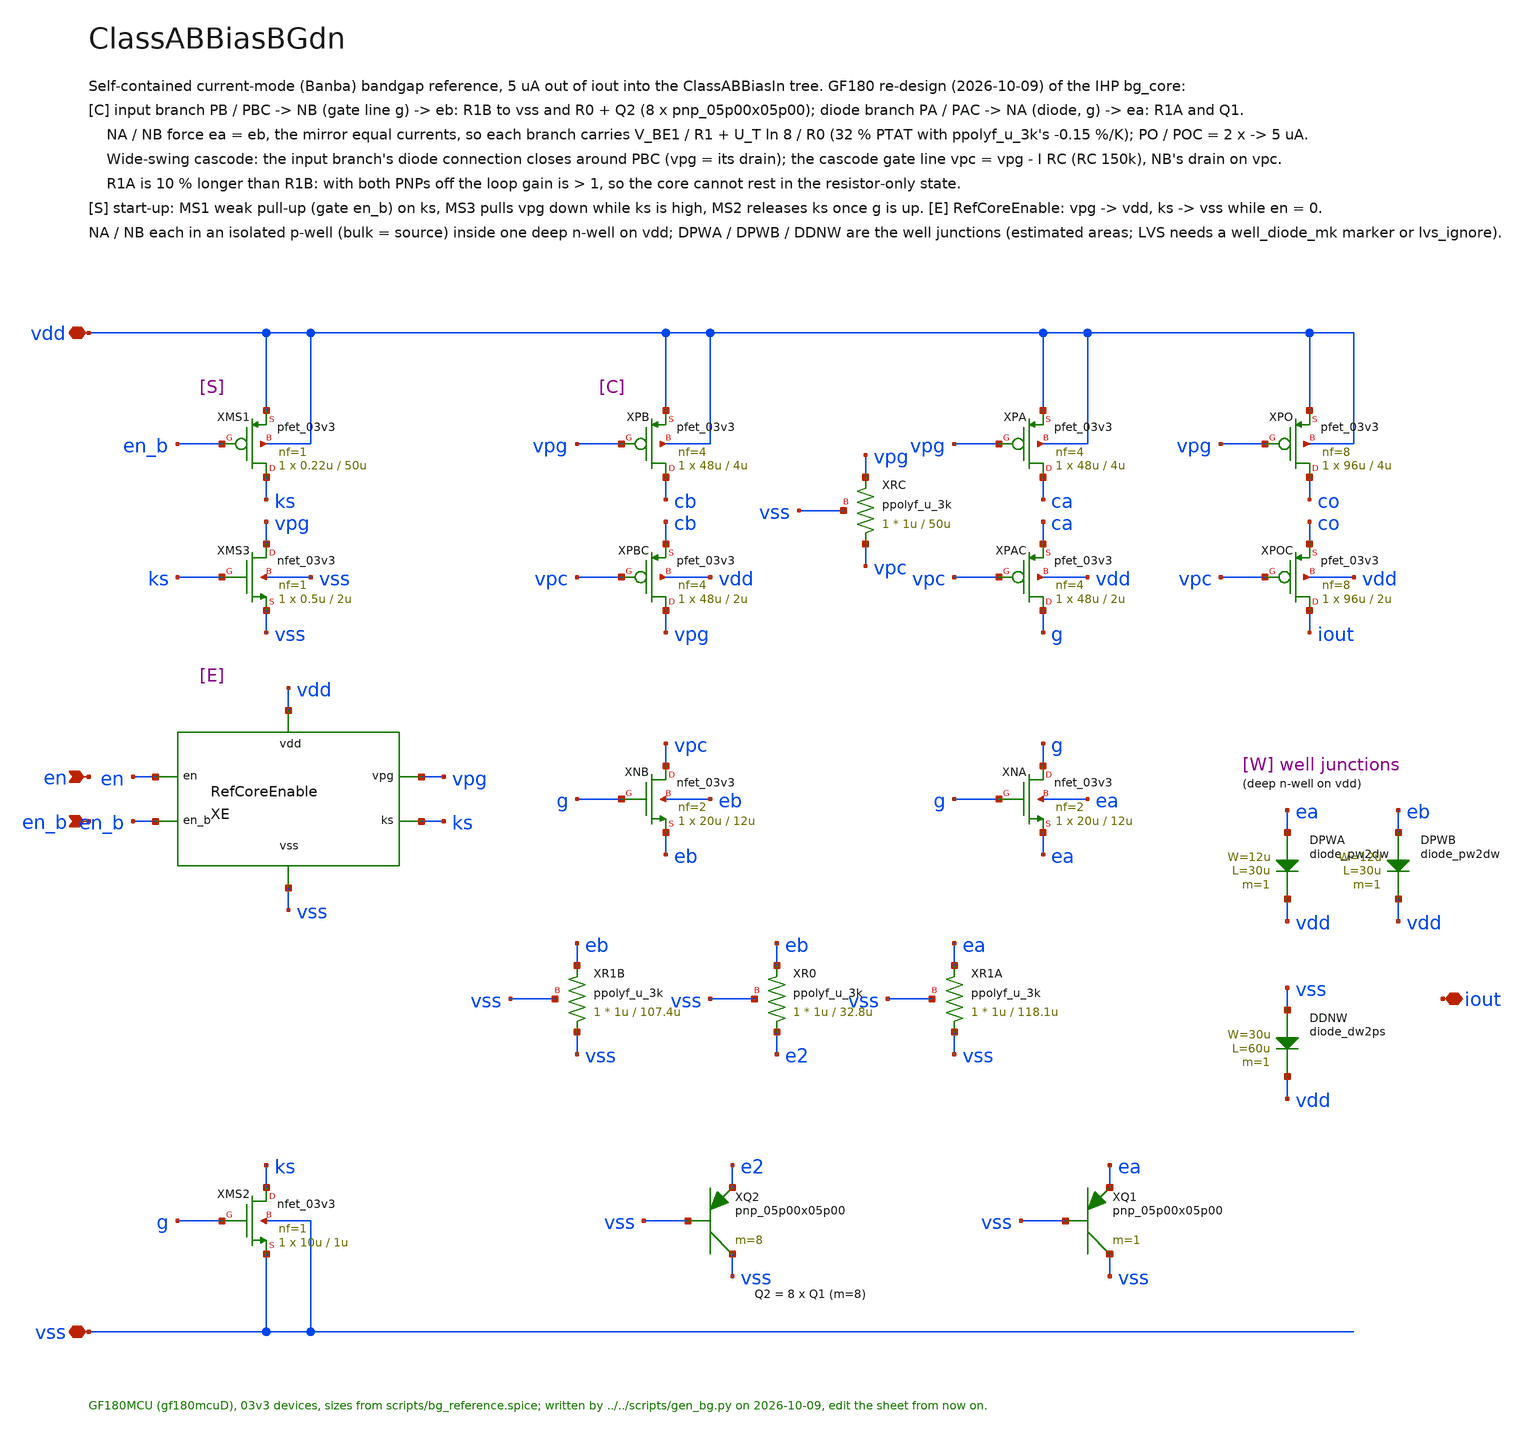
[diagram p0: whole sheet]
** sch_path: macros/ClassABBias/schematic/xschem/ClassABBiasBGdn.sch
**.subckt ClassABBiasBGdn vdd vss en en_b iout
*.iopin vdd
*.iopin vss
*.ipin en
*.ipin en_b
*.iopin iout
XE vdd vss en en_b vpg ks RefCoreEnable
XMS1 ks en_b vdd vdd pfet_03v3 L=50u W=0.22u nf=1 ad='int((nf+1)/2) * W/nf * 0.18u' as='int((nf+2)/2) * W/nf * 0.18u'
+ pd='2*int((nf+1)/2) * (W/nf + 0.18u)' ps='2*int((nf+2)/2) * (W/nf + 0.18u)' nrd='0.18u / W' nrs='0.18u / W'
+ sa=0 sb=0 sd=0 m=1
XMS3 vpg ks vss vss nfet_03v3 L=2u W=0.5u nf=1 ad='int((nf+1)/2) * W/nf * 0.18u' as='int((nf+2)/2) * W/nf * 0.18u'
+ pd='2*int((nf+1)/2) * (W/nf + 0.18u)' ps='2*int((nf+2)/2) * (W/nf + 0.18u)' nrd='0.18u / W' nrs='0.18u / W'
+ sa=0 sb=0 sd=0 m=1
XMS2 ks g vss vss nfet_03v3 L=1u W=10u nf=1 ad='int((nf+1)/2) * W/nf * 0.18u' as='int((nf+2)/2) * W/nf * 0.18u'
+ pd='2*int((nf+1)/2) * (W/nf + 0.18u)' ps='2*int((nf+2)/2) * (W/nf + 0.18u)' nrd='0.18u / W' nrs='0.18u / W'
+ sa=0 sb=0 sd=0 m=1
XPB cb vpg vdd vdd pfet_03v3 L=4u W=48u nf=4 ad='int((nf+1)/2) * W/nf * 0.18u' as='int((nf+2)/2) * W/nf * 0.18u'
+ pd='2*int((nf+1)/2) * (W/nf + 0.18u)' ps='2*int((nf+2)/2) * (W/nf + 0.18u)' nrd='0.18u / W' nrs='0.18u / W'
+ sa=0 sb=0 sd=0 m=1
XPBC vpg vpc cb vdd pfet_03v3 L=2u W=48u nf=4 ad='int((nf+1)/2) * W/nf * 0.18u' as='int((nf+2)/2) * W/nf * 0.18u'
+ pd='2*int((nf+1)/2) * (W/nf + 0.18u)' ps='2*int((nf+2)/2) * (W/nf + 0.18u)' nrd='0.18u / W' nrs='0.18u / W'
+ sa=0 sb=0 sd=0 m=1
XNB vpc g eb eb nfet_03v3 L=12u W=20u nf=2 ad='int((nf+1)/2) * W/nf * 0.18u' as='int((nf+2)/2) * W/nf * 0.18u'
+ pd='2*int((nf+1)/2) * (W/nf + 0.18u)' ps='2*int((nf+2)/2) * (W/nf + 0.18u)' nrd='0.18u / W' nrs='0.18u / W'
+ sa=0 sb=0 sd=0 m=1
XR1B vss eb vss ppolyf_u_3k r_width=1u r_length=107.4u m=1
XR0 e2 eb vss ppolyf_u_3k r_width=1u r_length=32.8u m=1
XQ2 vss vss e2 pnp_05p00x05p00 m=8 par=8
XRC vpc vpg vss ppolyf_u_3k r_width=1u r_length=50u m=1
XPA ca vpg vdd vdd pfet_03v3 L=4u W=48u nf=4 ad='int((nf+1)/2) * W/nf * 0.18u' as='int((nf+2)/2) * W/nf * 0.18u'
+ pd='2*int((nf+1)/2) * (W/nf + 0.18u)' ps='2*int((nf+2)/2) * (W/nf + 0.18u)' nrd='0.18u / W' nrs='0.18u / W'
+ sa=0 sb=0 sd=0 m=1
XPAC g vpc ca vdd pfet_03v3 L=2u W=48u nf=4 ad='int((nf+1)/2) * W/nf * 0.18u' as='int((nf+2)/2) * W/nf * 0.18u'
+ pd='2*int((nf+1)/2) * (W/nf + 0.18u)' ps='2*int((nf+2)/2) * (W/nf + 0.18u)' nrd='0.18u / W' nrs='0.18u / W'
+ sa=0 sb=0 sd=0 m=1
XNA g g ea ea nfet_03v3 L=12u W=20u nf=2 ad='int((nf+1)/2) * W/nf * 0.18u' as='int((nf+2)/2) * W/nf * 0.18u'
+ pd='2*int((nf+1)/2) * (W/nf + 0.18u)' ps='2*int((nf+2)/2) * (W/nf + 0.18u)' nrd='0.18u / W' nrs='0.18u / W'
+ sa=0 sb=0 sd=0 m=1
XR1A vss ea vss ppolyf_u_3k r_width=1u r_length=118.1u m=1
XQ1 vss vss ea pnp_05p00x05p00 m=1 par=1
XPO co vpg vdd vdd pfet_03v3 L=4u W=96u nf=8 ad='int((nf+1)/2) * W/nf * 0.18u' as='int((nf+2)/2) * W/nf * 0.18u'
+ pd='2*int((nf+1)/2) * (W/nf + 0.18u)' ps='2*int((nf+2)/2) * (W/nf + 0.18u)' nrd='0.18u / W' nrs='0.18u / W'
+ sa=0 sb=0 sd=0 m=1
XPOC iout vpc co vdd pfet_03v3 L=2u W=96u nf=8 ad='int((nf+1)/2) * W/nf * 0.18u' as='int((nf+2)/2) * W/nf * 0.18u'
+ pd='2*int((nf+1)/2) * (W/nf + 0.18u)' ps='2*int((nf+2)/2) * (W/nf + 0.18u)' nrd='0.18u / W' nrs='0.18u / W'
+ sa=0 sb=0 sd=0 m=1
DPWA ea vdd diode_pw2dw area='12u * 30u ' pj='2*12u + 2*30u ' m=1
DPWB eb vdd diode_pw2dw area='12u * 30u ' pj='2*12u + 2*30u ' m=1
DDNW vss vdd diode_dw2ps area='30u * 60u ' pj='2*30u + 2*60u ' m=1
**.ends

* expanding   symbol:  RefCoreEnable.sym # of pins=6
** sym_path: macros/PadEnable/schematic/xschem/RefCoreEnable.sym
** sch_path: macros/PadEnable/schematic/xschem/RefCoreEnable.sch
.subckt RefCoreEnable vdd vss en en_b vpg ks
*.iopin vdd
*.iopin vss
*.ipin en
*.ipin en_b
*.iopin vpg
*.iopin ks
XSPG vpg en vdd vdd pfet_03v3 L=0.5u W=1u nf=1 ad='int((nf+1)/2) * W/nf * 0.18u' as='int((nf+2)/2) * W/nf * 0.18u'
+ pd='2*int((nf+1)/2) * (W/nf + 0.18u)' ps='2*int((nf+2)/2) * (W/nf + 0.18u)' nrd='0.18u / W' nrs='0.18u / W'
+ sa=0 sb=0 sd=0 m=1
XSKS ks en_b vss vss nfet_03v3 L=0.5u W=1u nf=1 ad='int((nf+1)/2) * W/nf * 0.18u' as='int((nf+2)/2) * W/nf * 0.18u'
+ pd='2*int((nf+1)/2) * (W/nf + 0.18u)' ps='2*int((nf+2)/2) * (W/nf + 0.18u)' nrd='0.18u / W' nrs='0.18u / W'
+ sa=0 sb=0 sd=0 m=1
.ends

.end
